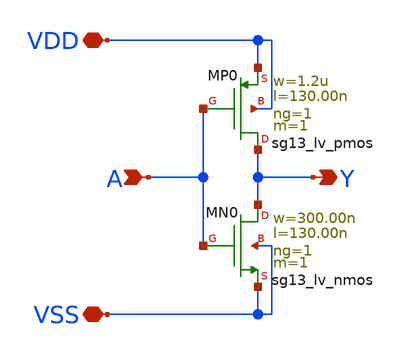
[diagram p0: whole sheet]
** sch_path: xschem/inv_1.sch
**.subckt inv_1 Y A VDD VSS
*.opin Y
*.ipin A
*.iopin VDD
*.iopin VSS
XMN0 Y A VSS VSS sg13_lv_nmos w=300.00n l=130.00n ng=1 m=1 mm_ok=1
XMP0 Y A VDD VDD sg13_lv_pmos w=1.2u l=130.00n ng=1 m=1 mm_ok=1
**.ends
.end
